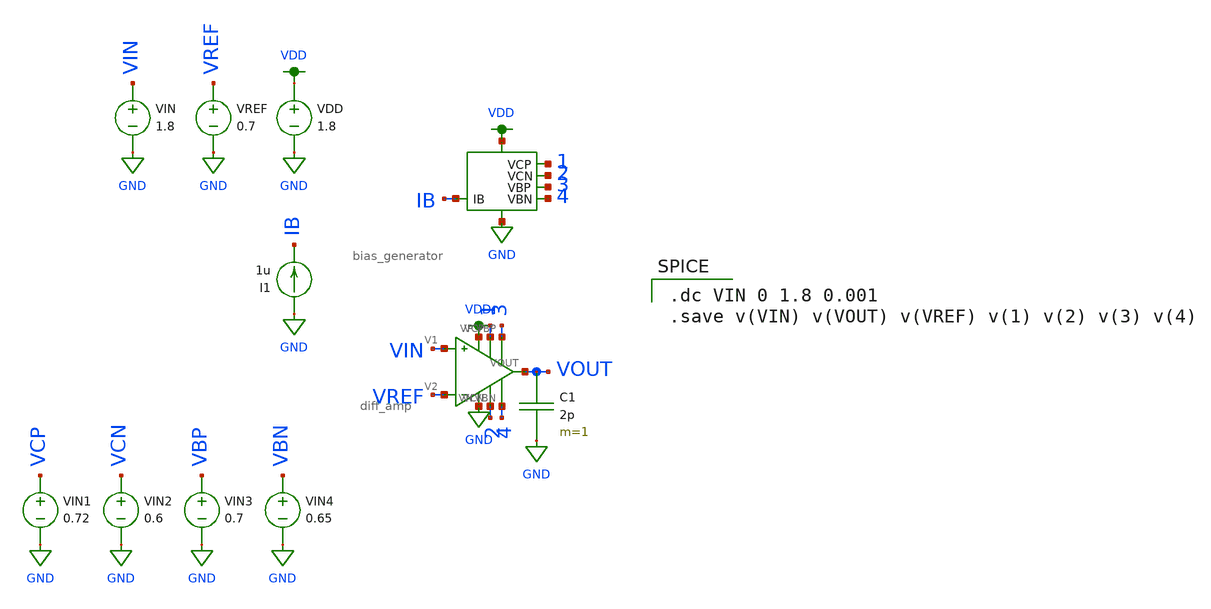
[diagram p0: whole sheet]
** sch_path: mp3/schematics/bias_generator_tran.sch
**.subckt bias_generator_tran
X1 IB VDD GND 2 1 3 4 bias_generator
VDD VDD GND 1.8
I1 GND IB 1u
VREF VREF GND 0.7
VIN VIN GND 1.8
X1 VIN VREF VDD GND 2 4 3 1 VOUT diff_amp
C1 VOUT GND 2p m=1
VIN1 VCP GND 0.72
VIN2 VCN GND 0.6
VIN3 VBP GND 0.7
VIN4 VBN GND 0.65
**** begin user architecture code

.option wnflag=1
.lib ~/skywater/skywater-pdk/libraries/sky130_fd_pr_ngspice/latest/models/sky130.lib.spice tt


.dc VIN 0 1.8 0.001
.save v(VIN) v(VOUT) v(VREF) v(1) v(2) v(3) v(4)

**** end user architecture code
**.ends

* expanding   symbol:  /home/madvlsi/Documents/VLSI/mp3/schematics/bias_generator.sym # of pins=7
** sym_path: mp3/schematics/bias_generator.sym
** sch_path: mp3/schematics/bias_generator.sch
.subckt bias_generator IB VP VN VCN VCP VBP VBN
*.iopin VP
*.iopin VN
*.iopin IB
*.iopin VBP
*.iopin VCN
*.iopin VCP
*.iopin VBN
XM12 VBN VBP VP VP sky130_fd_pr__pfet_01v8 L=1.5 W=12 nf=1 ad='int((nf+1)/2) * W/nf * 0.29' as='int((nf+2)/2) * W/nf * 0.29'
+ pd='2*int((nf+1)/2) * (W/nf + 0.29)' ps='2*int((nf+2)/2) * (W/nf + 0.29)' nrd='0.29 / W' nrs='0.29 / W'
+ sa=0 sb=0 sd=0 mult=1 m=1
XM13 VCN VBP VP VP sky130_fd_pr__pfet_01v8 L=0.5 W=12 nf=1 ad='int((nf+1)/2) * W/nf * 0.29' as='int((nf+2)/2) * W/nf * 0.29'
+ pd='2*int((nf+1)/2) * (W/nf + 0.29)' ps='2*int((nf+2)/2) * (W/nf + 0.29)' nrd='0.29 / W' nrs='0.29 / W'
+ sa=0 sb=0 sd=0 mult=1 m=1
XM19 net3 net3 net2 VP sky130_fd_pr__pfet_01v8 L=0.5 W=24 nf=1 ad='int((nf+1)/2) * W/nf * 0.29' as='int((nf+2)/2) * W/nf * 0.29'
+ pd='2*int((nf+1)/2) * (W/nf + 0.29)' ps='2*int((nf+2)/2) * (W/nf + 0.29)' nrd='0.29 / W' nrs='0.29 / W'
+ sa=0 sb=0 sd=0 mult=1 m=1
XM20 VCP VCP net2 VP sky130_fd_pr__pfet_01v8 L=0.5 W=12 nf=1 ad='int((nf+1)/2) * W/nf * 0.29' as='int((nf+2)/2) * W/nf * 0.29'
+ pd='2*int((nf+1)/2) * (W/nf + 0.29)' ps='2*int((nf+2)/2) * (W/nf + 0.29)' nrd='0.29 / W' nrs='0.29 / W'
+ sa=0 sb=0 sd=0 mult=1 m=1
XM18 net2 net3 VP VP sky130_fd_pr__pfet_01v8 L=0.5 W=12 nf=1 ad='int((nf+1)/2) * W/nf * 0.29' as='int((nf+2)/2) * W/nf * 0.29'
+ pd='2*int((nf+1)/2) * (W/nf + 0.29)' ps='2*int((nf+2)/2) * (W/nf + 0.29)' nrd='0.29 / W' nrs='0.29 / W'
+ sa=0 sb=0 sd=0 mult=1 m=1
XM22 VCP IB VN VN sky130_fd_pr__nfet_01v8 L=0.5 W=12 nf=1 ad='int((nf+1)/2) * W/nf * 0.29' as='int((nf+2)/2) * W/nf * 0.29'
+ pd='2*int((nf+1)/2) * (W/nf + 0.29)' ps='2*int((nf+2)/2) * (W/nf + 0.29)' nrd='0.29 / W' nrs='0.29 / W'
+ sa=0 sb=0 sd=0 mult=1 m=1
XM21 net3 IB VN VN sky130_fd_pr__nfet_01v8 L=1.5 W=12 nf=1 ad='int((nf+1)/2) * W/nf * 0.29' as='int((nf+2)/2) * W/nf * 0.29'
+ pd='2*int((nf+1)/2) * (W/nf + 0.29)' ps='2*int((nf+2)/2) * (W/nf + 0.29)' nrd='0.29 / W' nrs='0.29 / W'
+ sa=0 sb=0 sd=0 mult=1 m=1
XM23 VBP IB VN VN sky130_fd_pr__nfet_01v8 L=0.5 W=12 nf=1 ad='int((nf+1)/2) * W/nf * 0.29' as='int((nf+2)/2) * W/nf * 0.29'
+ pd='2*int((nf+1)/2) * (W/nf + 0.29)' ps='2*int((nf+2)/2) * (W/nf + 0.29)' nrd='0.29 / W' nrs='0.29 / W'
+ sa=0 sb=0 sd=0 mult=1 m=1
XM24 IB IB VN VN sky130_fd_pr__nfet_01v8 L=0.5 W=12 nf=1 ad='int((nf+1)/2) * W/nf * 0.29' as='int((nf+2)/2) * W/nf * 0.29'
+ pd='2*int((nf+1)/2) * (W/nf + 0.29)' ps='2*int((nf+2)/2) * (W/nf + 0.29)' nrd='0.29 / W' nrs='0.29 / W'
+ sa=0 sb=0 sd=0 mult=1 m=1
XM15 VCN VCN net1 VN sky130_fd_pr__nfet_01v8 L=0.5 W=12 nf=1 ad='int((nf+1)/2) * W/nf * 0.29' as='int((nf+2)/2) * W/nf * 0.29'
+ pd='2*int((nf+1)/2) * (W/nf + 0.29)' ps='2*int((nf+2)/2) * (W/nf + 0.29)' nrd='0.29 / W' nrs='0.29 / W'
+ sa=0 sb=0 sd=0 mult=1 m=1
XM14 VBN VBN net1 VN sky130_fd_pr__nfet_01v8 L=0.5 W=24 nf=1 ad='int((nf+1)/2) * W/nf * 0.29' as='int((nf+2)/2) * W/nf * 0.29'
+ pd='2*int((nf+1)/2) * (W/nf + 0.29)' ps='2*int((nf+2)/2) * (W/nf + 0.29)' nrd='0.29 / W' nrs='0.29 / W'
+ sa=0 sb=0 sd=0 mult=1 m=1
XM16 net1 VBN VN VN sky130_fd_pr__nfet_01v8 L=0.5 W=12 nf=1 ad='int((nf+1)/2) * W/nf * 0.29' as='int((nf+2)/2) * W/nf * 0.29'
+ pd='2*int((nf+1)/2) * (W/nf + 0.29)' ps='2*int((nf+2)/2) * (W/nf + 0.29)' nrd='0.29 / W' nrs='0.29 / W'
+ sa=0 sb=0 sd=0 mult=1 m=1
XM17 VBP VBP VP VP sky130_fd_pr__pfet_01v8 L=0.5 W=12 nf=1 ad='int((nf+1)/2) * W/nf * 0.29' as='int((nf+2)/2) * W/nf * 0.29'
+ pd='2*int((nf+1)/2) * (W/nf + 0.29)' ps='2*int((nf+2)/2) * (W/nf + 0.29)' nrd='0.29 / W' nrs='0.29 / W'
+ sa=0 sb=0 sd=0 mult=1 m=1
.ends


* expanding   symbol:  /home/madvlsi/Documents/VLSI/mp3/schematics/diff_amp.sym # of pins=9
** sym_path: mp3/schematics/diff_amp.sym
** sch_path: mp3/schematics/diff_amp.sch
.subckt diff_amp V1 V2 VP VN VCN VBN VBP VCP VOUT
*.ipin V1
*.ipin V2
*.iopin VP
*.iopin VN
*.opin VOUT
*.iopin VBP
*.iopin VCP
*.iopin VCN
*.iopin VBN
XM1 net1 VBP VP VP sky130_fd_pr__pfet_01v8 L=0.5 W=12 nf=1 ad='int((nf+1)/2) * W/nf * 0.29' as='int((nf+2)/2) * W/nf * 0.29'
+ pd='2*int((nf+1)/2) * (W/nf + 0.29)' ps='2*int((nf+2)/2) * (W/nf + 0.29)' nrd='0.29 / W' nrs='0.29 / W'
+ sa=0 sb=0 sd=0 mult=1 m=1
XM5 net3 VCN net4 VN sky130_fd_pr__nfet_01v8 L=0.5 W=12 nf=1 ad='int((nf+1)/2) * W/nf * 0.29' as='int((nf+2)/2) * W/nf * 0.29'
+ pd='2*int((nf+1)/2) * (W/nf + 0.29)' ps='2*int((nf+2)/2) * (W/nf + 0.29)' nrd='0.29 / W' nrs='0.29 / W'
+ sa=0 sb=0 sd=0 mult=1 m=1
XM2 net2 VBP VP VP sky130_fd_pr__pfet_01v8 L=0.5 W=12 nf=1 ad='int((nf+1)/2) * W/nf * 0.29' as='int((nf+2)/2) * W/nf * 0.29'
+ pd='2*int((nf+1)/2) * (W/nf + 0.29)' ps='2*int((nf+2)/2) * (W/nf + 0.29)' nrd='0.29 / W' nrs='0.29 / W'
+ sa=0 sb=0 sd=0 mult=1 m=1
XM3 VOUT VCP net2 VP sky130_fd_pr__pfet_01v8 L=0.5 W=12 nf=1 ad='int((nf+1)/2) * W/nf * 0.29' as='int((nf+2)/2) * W/nf * 0.29'
+ pd='2*int((nf+1)/2) * (W/nf + 0.29)' ps='2*int((nf+2)/2) * (W/nf + 0.29)' nrd='0.29 / W' nrs='0.29 / W'
+ sa=0 sb=0 sd=0 mult=1 m=1
XM4 net3 VCP net1 VP sky130_fd_pr__pfet_01v8 L=0.5 W=12 nf=1 ad='int((nf+1)/2) * W/nf * 0.29' as='int((nf+2)/2) * W/nf * 0.29'
+ pd='2*int((nf+1)/2) * (W/nf + 0.29)' ps='2*int((nf+2)/2) * (W/nf + 0.29)' nrd='0.29 / W' nrs='0.29 / W'
+ sa=0 sb=0 sd=0 mult=1 m=1
XM6 net1 V1 net6 VN sky130_fd_pr__nfet_01v8 L=0.5 W=12 nf=1 ad='int((nf+1)/2) * W/nf * 0.29' as='int((nf+2)/2) * W/nf * 0.29'
+ pd='2*int((nf+1)/2) * (W/nf + 0.29)' ps='2*int((nf+2)/2) * (W/nf + 0.29)' nrd='0.29 / W' nrs='0.29 / W'
+ sa=0 sb=0 sd=0 mult=1 m=1
XM7 net2 V2 net6 VN sky130_fd_pr__nfet_01v8 L=0.5 W=12 nf=1 ad='int((nf+1)/2) * W/nf * 0.29' as='int((nf+2)/2) * W/nf * 0.29'
+ pd='2*int((nf+1)/2) * (W/nf + 0.29)' ps='2*int((nf+2)/2) * (W/nf + 0.29)' nrd='0.29 / W' nrs='0.29 / W'
+ sa=0 sb=0 sd=0 mult=1 m=1
XM8 VOUT VCN net5 VN sky130_fd_pr__nfet_01v8 L=0.5 W=12 nf=1 ad='int((nf+1)/2) * W/nf * 0.29' as='int((nf+2)/2) * W/nf * 0.29'
+ pd='2*int((nf+1)/2) * (W/nf + 0.29)' ps='2*int((nf+2)/2) * (W/nf + 0.29)' nrd='0.29 / W' nrs='0.29 / W'
+ sa=0 sb=0 sd=0 mult=1 m=1
XM9 net5 net3 VN VN sky130_fd_pr__nfet_01v8 L=0.5 W=12 nf=1 ad='int((nf+1)/2) * W/nf * 0.29' as='int((nf+2)/2) * W/nf * 0.29'
+ pd='2*int((nf+1)/2) * (W/nf + 0.29)' ps='2*int((nf+2)/2) * (W/nf + 0.29)' nrd='0.29 / W' nrs='0.29 / W'
+ sa=0 sb=0 sd=0 mult=1 m=1
XM10 net4 net3 VN VN sky130_fd_pr__nfet_01v8 L=0.5 W=12 nf=1 ad='int((nf+1)/2) * W/nf * 0.29' as='int((nf+2)/2) * W/nf * 0.29'
+ pd='2*int((nf+1)/2) * (W/nf + 0.29)' ps='2*int((nf+2)/2) * (W/nf + 0.29)' nrd='0.29 / W' nrs='0.29 / W'
+ sa=0 sb=0 sd=0 mult=1 m=1
XM11 net6 VBN VN VN sky130_fd_pr__nfet_01v8 L=0.5 W=12 nf=1 ad='int((nf+1)/2) * W/nf * 0.29' as='int((nf+2)/2) * W/nf * 0.29'
+ pd='2*int((nf+1)/2) * (W/nf + 0.29)' ps='2*int((nf+2)/2) * (W/nf + 0.29)' nrd='0.29 / W' nrs='0.29 / W'
+ sa=0 sb=0 sd=0 mult=1 m=1
.ends

.GLOBAL GND
.GLOBAL VDD
.end
